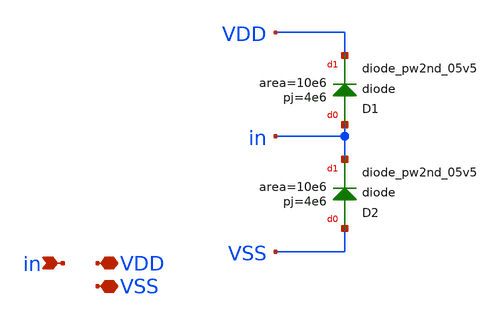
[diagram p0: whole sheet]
** sch_path: xschem/src/esd_diodes/esd_diodes.sch
**.subckt esd_diodes VDD in VSS
*.iopin VDD
*.ipin in
*.iopin VSS
XD1 in VDD sky130_fd_pr__diode_pw2nd_05v5 area=10e6 pj=4e6
XD2 VSS in sky130_fd_pr__diode_pw2nd_05v5 area=10e6 pj=4e6
**.ends
.end
